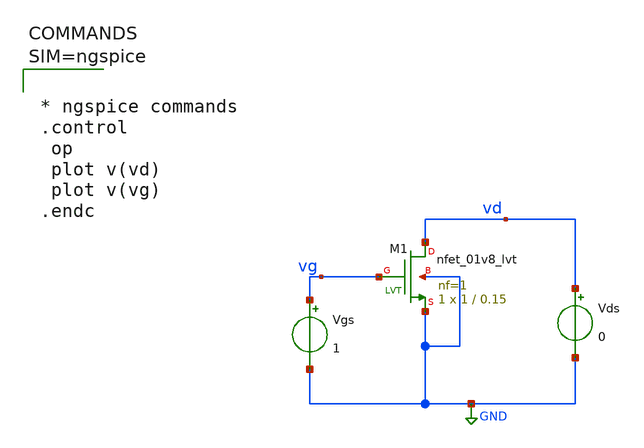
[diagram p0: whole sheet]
** sch_path: xschem/nfet_M1.sch
**.subckt nfet_M1
XM1 vd vg GND GND sky130_fd_pr__nfet_01v8_lvt L=0.15 W=1 nf=1 ad='int((1 + 1)/2) * 1 / 1 * 0.29' as='int((1 + 2)/2) * 1 / 1 * 0.29'
+ pd='2*int((1 + 1)/2) * (1 / 1 + 0.29)' ps='2*int((1 + 2)/2) * (1 / 1 + 0.29)' nrd='0.29 / 1 ' nrs='0.29 / 1 '
+ sa=0 sb=0 sd=0 mult=1 m=1
Vgs vg GND 1
Vds vd GND 0
**** begin user architecture code

** opencircuitdesign pdks install
.lib $::SKYWATER_MODELS/sky130.lib.spice tt




* ngspice commands
.control
 op
 plot v(vd)
 plot v(vg)
.endc



**** end user architecture code
**.ends
.GLOBAL GND
.end
